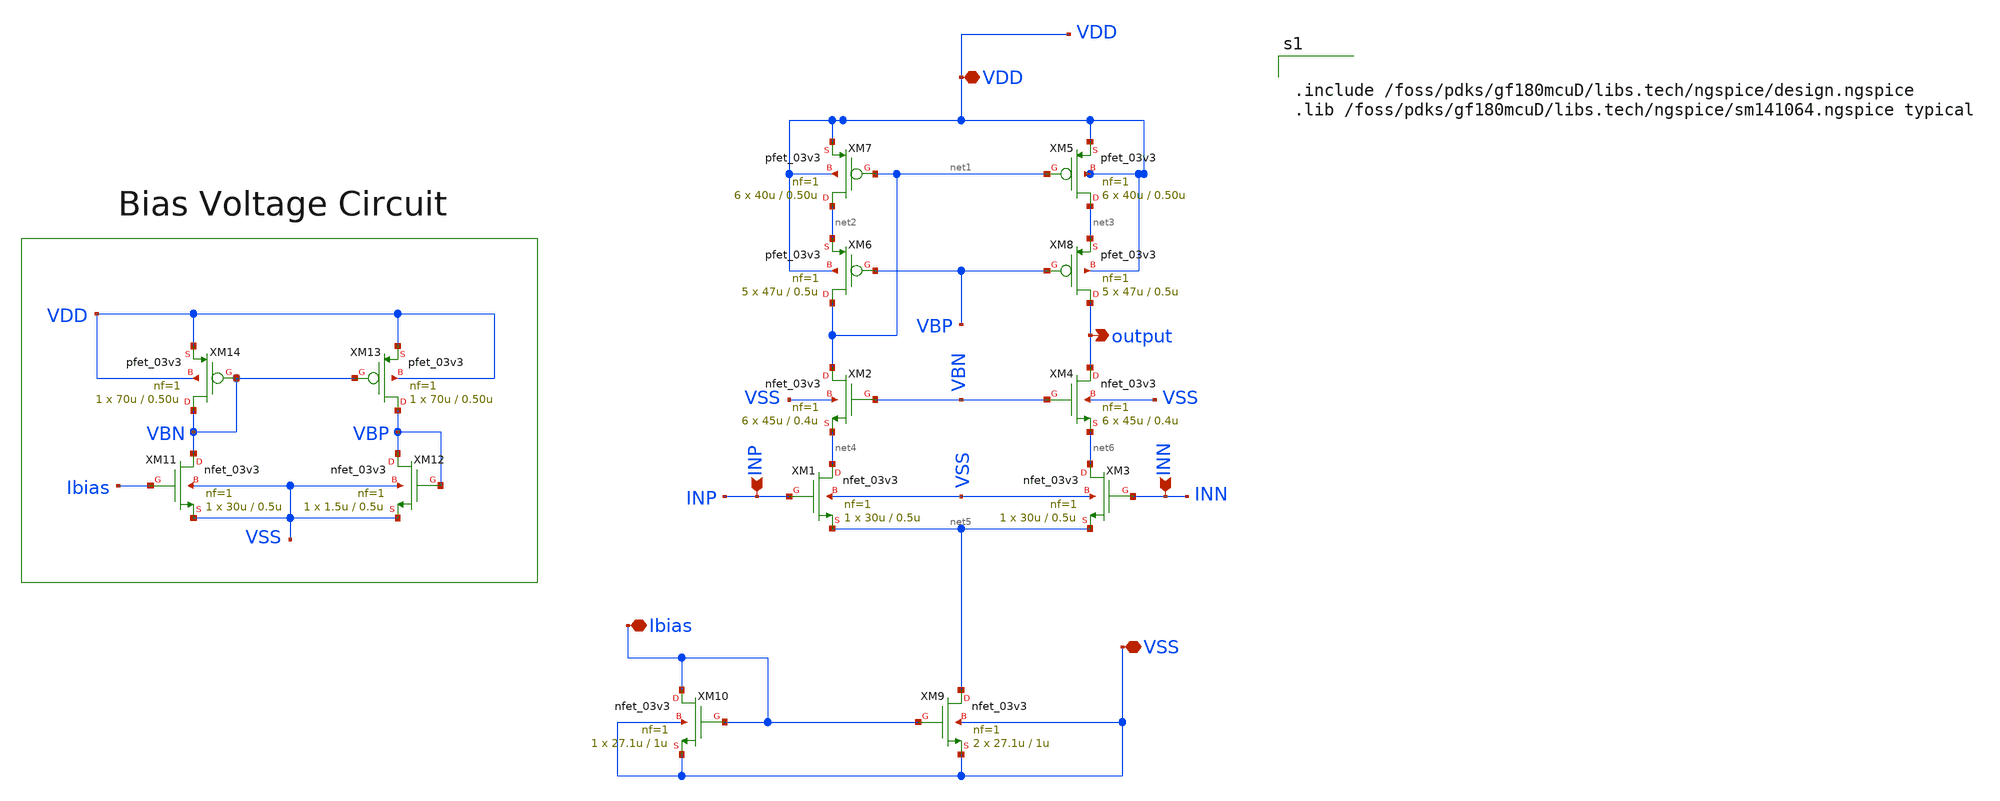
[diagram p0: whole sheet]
** sch_path: designs/libs/core_amps/ota_telescopic/ota_telescopic schematics/telescopic_cascode.sch
**.subckt telescopic_cascode INP INN output Ibias VDD VSS
*.ipin INP
*.ipin INN
*.opin output
*.iopin Ibias
*.iopin VDD
*.iopin VSS
XM8 output VBP net3 VDD pfet_03v3 L=0.5u W=47u nf=1 ad='int((nf+1)/2) * W/nf * 0.18u' as='int((nf+2)/2) * W/nf * 0.18u'
+ pd='2*int((nf+1)/2) * (W/nf + 0.18u)' ps='2*int((nf+2)/2) * (W/nf + 0.18u)' nrd='0.18u / W' nrs='0.18u / W'
+ sa=0 sb=0 sd=0 m=5
XM4 output VBN net6 VSS nfet_03v3 L=0.4u W=45u nf=1 ad='int((nf+1)/2) * W/nf * 0.18u' as='int((nf+2)/2) * W/nf * 0.18u'
+ pd='2*int((nf+1)/2) * (W/nf + 0.18u)' ps='2*int((nf+2)/2) * (W/nf + 0.18u)' nrd='0.18u / W' nrs='0.18u / W'
+ sa=0 sb=0 sd=0 m=6
XM1 net4 INP net5 VSS nfet_03v3 L=0.5u W=30u nf=1 ad='int((nf+1)/2) * W/nf * 0.18u' as='int((nf+2)/2) * W/nf * 0.18u'
+ pd='2*int((nf+1)/2) * (W/nf + 0.18u)' ps='2*int((nf+2)/2) * (W/nf + 0.18u)' nrd='0.18u / W' nrs='0.18u / W'
+ sa=0 sb=0 sd=0 m=1
XM2 net1 VBN net4 VSS nfet_03v3 L=0.4u W=45u nf=1 ad='int((nf+1)/2) * W/nf * 0.18u' as='int((nf+2)/2) * W/nf * 0.18u'
+ pd='2*int((nf+1)/2) * (W/nf + 0.18u)' ps='2*int((nf+2)/2) * (W/nf + 0.18u)' nrd='0.18u / W' nrs='0.18u / W'
+ sa=0 sb=0 sd=0 m=6
XM3 net6 INN net5 VSS nfet_03v3 L=0.5u W=30u nf=1 ad='int((nf+1)/2) * W/nf * 0.18u' as='int((nf+2)/2) * W/nf * 0.18u'
+ pd='2*int((nf+1)/2) * (W/nf + 0.18u)' ps='2*int((nf+2)/2) * (W/nf + 0.18u)' nrd='0.18u / W' nrs='0.18u / W'
+ sa=0 sb=0 sd=0 m=1
XM5 net3 net1 VDD VDD pfet_03v3 L=0.50u W=40u nf=1 ad='int((nf+1)/2) * W/nf * 0.18u' as='int((nf+2)/2) * W/nf * 0.18u'
+ pd='2*int((nf+1)/2) * (W/nf + 0.18u)' ps='2*int((nf+2)/2) * (W/nf + 0.18u)' nrd='0.18u / W' nrs='0.18u / W'
+ sa=0 sb=0 sd=0 m=6
XM6 net1 VBP net2 VDD pfet_03v3 L=0.5u W=47u nf=1 ad='int((nf+1)/2) * W/nf * 0.18u' as='int((nf+2)/2) * W/nf * 0.18u'
+ pd='2*int((nf+1)/2) * (W/nf + 0.18u)' ps='2*int((nf+2)/2) * (W/nf + 0.18u)' nrd='0.18u / W' nrs='0.18u / W'
+ sa=0 sb=0 sd=0 m=5
XM7 net2 net1 VDD VDD pfet_03v3 L=0.50u W=40u nf=1 ad='int((nf+1)/2) * W/nf * 0.18u' as='int((nf+2)/2) * W/nf * 0.18u'
+ pd='2*int((nf+1)/2) * (W/nf + 0.18u)' ps='2*int((nf+2)/2) * (W/nf + 0.18u)' nrd='0.18u / W' nrs='0.18u / W'
+ sa=0 sb=0 sd=0 m=6
XM9 net5 Ibias VSS VSS nfet_03v3 L=1u W=27.1u nf=1 ad='int((nf+1)/2) * W/nf * 0.18u' as='int((nf+2)/2) * W/nf * 0.18u'
+ pd='2*int((nf+1)/2) * (W/nf + 0.18u)' ps='2*int((nf+2)/2) * (W/nf + 0.18u)' nrd='0.18u / W' nrs='0.18u / W'
+ sa=0 sb=0 sd=0 m=2
XM10 Ibias Ibias VSS VSS nfet_03v3 L=1u W=27.1u nf=1 ad='int((nf+1)/2) * W/nf * 0.18u' as='int((nf+2)/2) * W/nf * 0.18u'
+ pd='2*int((nf+1)/2) * (W/nf + 0.18u)' ps='2*int((nf+2)/2) * (W/nf + 0.18u)' nrd='0.18u / W' nrs='0.18u / W'
+ sa=0 sb=0 sd=0 m=1
XM11 VBN Ibias VSS VSS nfet_03v3 L=0.5u W=30u nf=1 ad='int((nf+1)/2) * W/nf * 0.18u' as='int((nf+2)/2) * W/nf * 0.18u'
+ pd='2*int((nf+1)/2) * (W/nf + 0.18u)' ps='2*int((nf+2)/2) * (W/nf + 0.18u)' nrd='0.18u / W' nrs='0.18u / W'
+ sa=0 sb=0 sd=0 m=1
XM12 VBP VBP VSS VSS nfet_03v3 L=0.5u W=1.5u nf=1 ad='int((nf+1)/2) * W/nf * 0.18u' as='int((nf+2)/2) * W/nf * 0.18u'
+ pd='2*int((nf+1)/2) * (W/nf + 0.18u)' ps='2*int((nf+2)/2) * (W/nf + 0.18u)' nrd='0.18u / W' nrs='0.18u / W'
+ sa=0 sb=0 sd=0 m=1
XM13 VBP VBN VDD VDD pfet_03v3 L=0.50u W=70u nf=1 ad='int((nf+1)/2) * W/nf * 0.18u' as='int((nf+2)/2) * W/nf * 0.18u'
+ pd='2*int((nf+1)/2) * (W/nf + 0.18u)' ps='2*int((nf+2)/2) * (W/nf + 0.18u)' nrd='0.18u / W' nrs='0.18u / W'
+ sa=0 sb=0 sd=0 m=1
XM14 VBN VBN VDD VDD pfet_03v3 L=0.50u W=70u nf=1 ad='int((nf+1)/2) * W/nf * 0.18u' as='int((nf+2)/2) * W/nf * 0.18u'
+ pd='2*int((nf+1)/2) * (W/nf + 0.18u)' ps='2*int((nf+2)/2) * (W/nf + 0.18u)' nrd='0.18u / W' nrs='0.18u / W'
+ sa=0 sb=0 sd=0 m=1
**** begin user architecture code


.include /foss/pdks/gf180mcuD/libs.tech/ngspice/design.ngspice
.lib /foss/pdks/gf180mcuD/libs.tech/ngspice/sm141064.ngspice typical

**** end user architecture code
**.ends
.end
